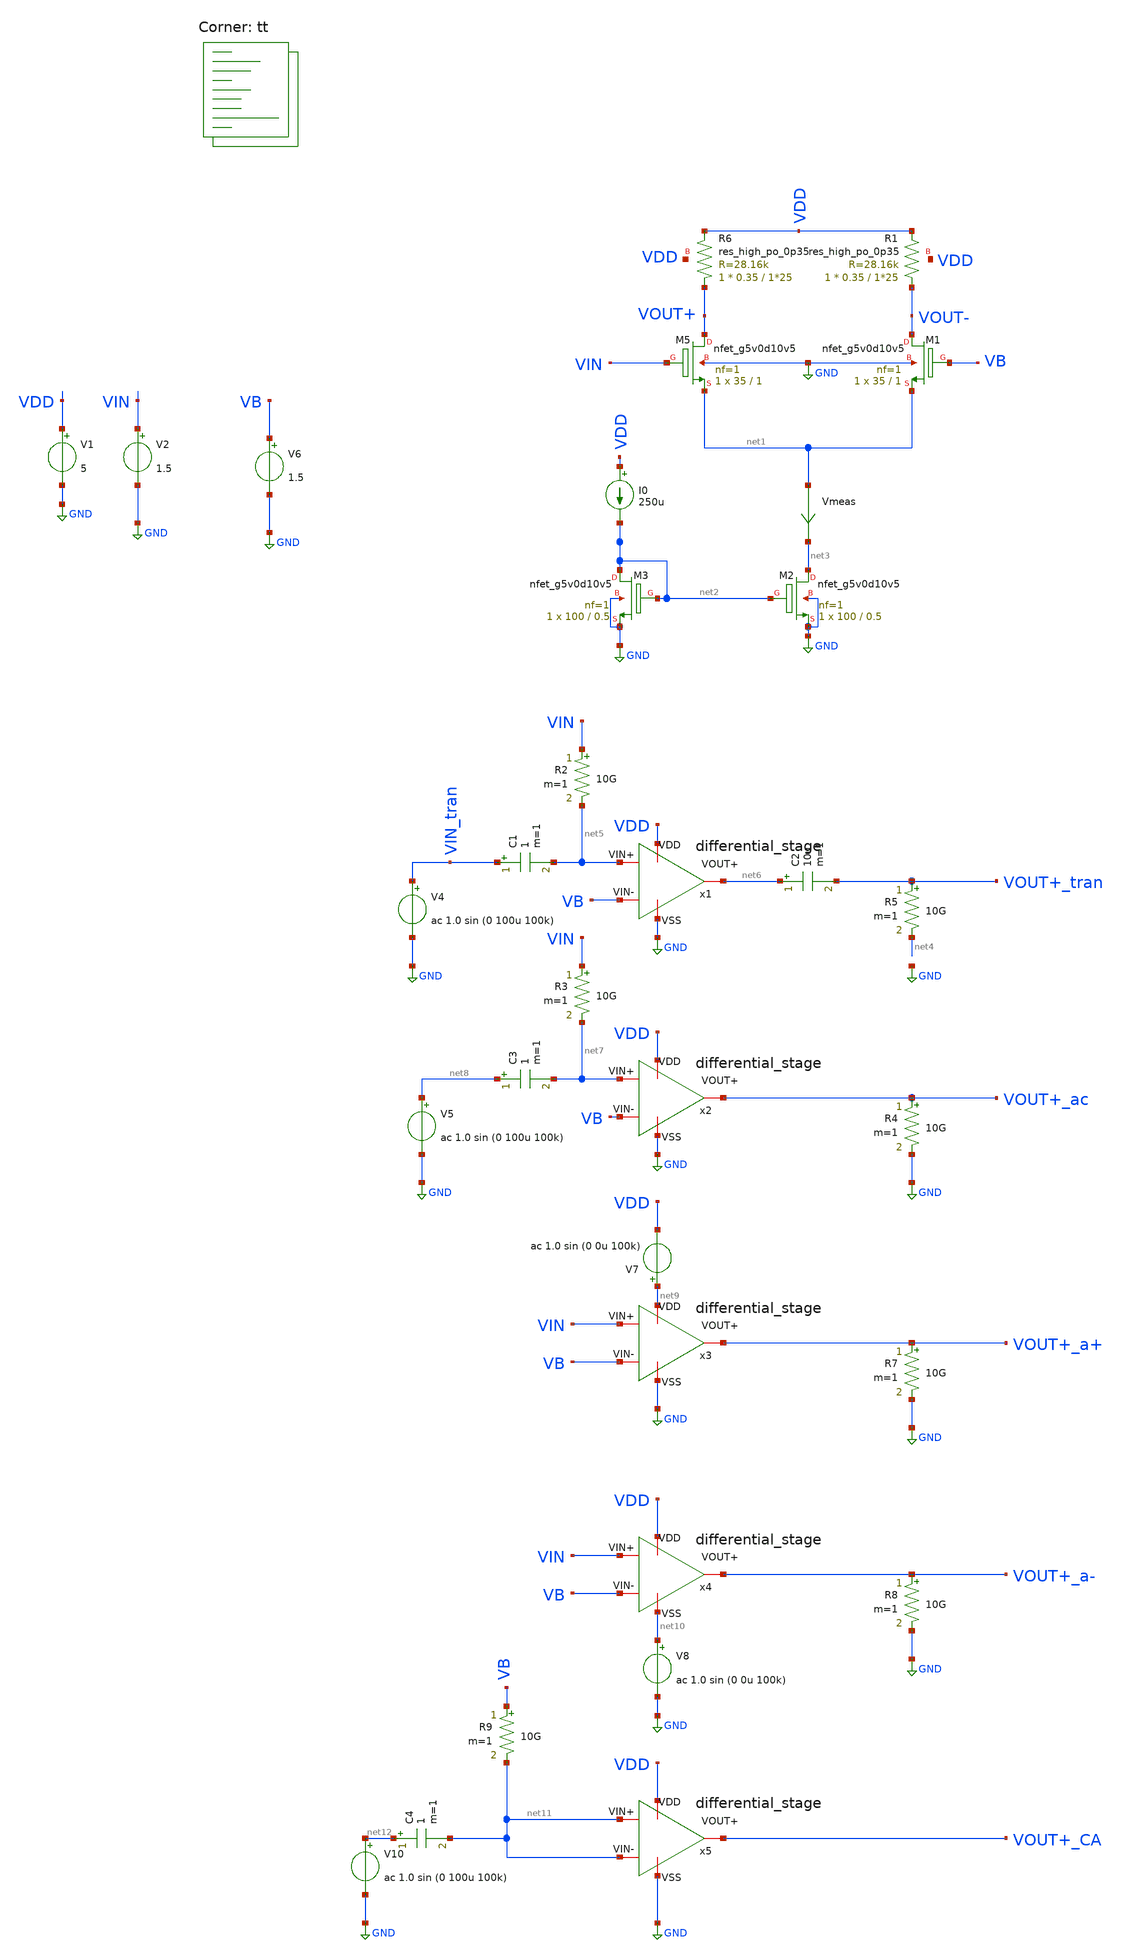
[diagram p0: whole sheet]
** sch_path: old stuff/amplifiers/differencial_stage_amps/basic_stages/basic_NMOS_resistive_stage/diferential_stage.sch
**.subckt diferential_stage
XM5 VOUT+ VIN net1 GND sky130_fd_pr__nfet_g5v0d10v5 L=1 W=35 nf=1 ad='int((1 + 1)/2) * 35 / 1 * 0.29'
+ as='int((1 + 2)/2) * 35 / 1 * 0.29' pd='2*int((1 + 1)/2) * (35 / 1 + 0.29)' ps='2*int((1 + 2)/2) * (35 / 1 + 0.29)'
+ nrd='0.29 / 35 ' nrs='0.29 / 35 ' sa=0 sb=0 sd=0 mult=1 m=1
XM1 VOUT- VB net1 GND sky130_fd_pr__nfet_g5v0d10v5 L=1 W=35 nf=1 ad='int((1 + 1)/2) * 35 / 1 * 0.29'
+ as='int((1 + 2)/2) * 35 / 1 * 0.29' pd='2*int((1 + 1)/2) * (35 / 1 + 0.29)' ps='2*int((1 + 2)/2) * (35 / 1 + 0.29)'
+ nrd='0.29 / 35 ' nrs='0.29 / 35 ' sa=0 sb=0 sd=0 mult=1 m=1
XR6 VOUT+ VDD VDD sky130_fd_pr__res_high_po_0p35 L=1*25 mult=1 m=1
XR1 VOUT- VDD VDD sky130_fd_pr__res_high_po_0p35 L=1*25 mult=1 m=1
V1 VDD GND 5
V2 VIN GND 1.5
V6 VB GND 1.5
XM2 net3 net2 GND GND sky130_fd_pr__nfet_g5v0d10v5 L=0.5 W=100 nf=1 ad='int((1 + 1)/2) * 100 / 1 * 0.29'
+ as='int((1 + 2)/2) * 100 / 1 * 0.29' pd='2*int((1 + 1)/2) * (100 / 1 + 0.29)' ps='2*int((1 + 2)/2) * (100 / 1 + 0.29)'
+ nrd='0.29 / 100 ' nrs='0.29 / 100 ' sa=0 sb=0 sd=0 mult=1 m=1
Vmeas net1 net3 0
.save i(vmeas)
R5 VOUT+_tran net4 10G m=1
R2 VIN net5 10G m=1
V4 VIN_tran GND ac 1.0 sin (0 100u 100k)
C2 net6 VOUT+_tran 10u m=1
C1 VIN_tran net5 1 m=1
R3 VIN net7 10G m=1
C3 net8 net7 1 m=1
V5 net8 GND ac 1.0 sin (0 100u 100k)
R4 VOUT+_ac GND 10G m=1
V7 net9 VDD ac 1.0 sin (0 0u 100k)
R7 VOUT+_a+ GND 10G m=1
V8 net10 GND ac 1.0 sin (0 0u 100k)
R8 VOUT+_a- GND 10G m=1
R9 VB net11 10G m=1
C4 net12 net11 1 m=1
V10 net12 GND ac 1.0 sin (0 100u 100k)
XM3 net2 net2 GND GND sky130_fd_pr__nfet_g5v0d10v5 L=0.5 W=100 nf=1 ad='int((1 + 1)/2) * 100 / 1 * 0.29'
+ as='int((1 + 2)/2) * 100 / 1 * 0.29' pd='2*int((1 + 1)/2) * (100 / 1 + 0.29)' ps='2*int((1 + 2)/2) * (100 / 1 + 0.29)'
+ nrd='0.29 / 100 ' nrs='0.29 / 100 ' sa=0 sb=0 sd=0 mult=1 m=1
I0 VDD net2 250u
x1 VDD GND net5 VB net6 differential_stage
x2 VDD GND net7 VB VOUT+_ac differential_stage
x3 net9 GND VIN VB VOUT+_a+ differential_stage
x4 VDD net10 VIN VB VOUT+_a- differential_stage
x5 VDD GND net11 net11 VOUT+_CA differential_stage
**** begin user architecture code

**************************************************************
**************************************************************
**************************************************************
**************************************************************
**************************************************************
*LIBs*********************************************************
**************************************************************
**************************************************************
**************************************************************
**************************************************************
**************************************************************
*.lib $::SKYWATER_MODELS/sky130.lib.spice tt
* chose the corners in the corner file
* tt_mm for mismatch
* ss ff sf fs standart corners
* ll hh lh hl capacitor and resistors corners
* mc for total process variation including corners
**************************************************************
**************************************************************
**************************************************************
**************************************************************
**************************************************************
*Corners/montecarlo options***********************************
**************************************************************
**************************************************************
**************************************************************
**************************************************************
**************************************************************
.TEMP 27
**************************************************************
**************************************************************
**************************************************************
**************************************************************
*SIMULATION and Plots*****************************************
**************************************************************
**************************************************************
**************************************************************
**************************************************************
.control
save all
dc V2 0 5 0.01
*dc simulation
plot v(VOUT-) v(VIN) deriv(v(VOUT-)) v(VOUT+) deriv(v(VOUT+))
*ploting VIN VOUT and the voltage gain
plot i(Vmeas)
*ploting the current for curiosity
tran 0.5ns 20u
*transient simulation
plot (v(VOUT+_tran)) v(VIN_tran)
*simple plot to exemplify the gain
fft v(VOUT+_tran) v(VIN_tran)
*fast fourier transfor
plot mag(v(VOUT+_tran)) mag(v(VIN_tran))
ac dec 20 1 1000G
*simple ac simulation
plot db(v(VOUT+_ac))
plot db(v(VOUT+_a+))
plot db(v(VOUT+_a-))
plot db(v(VOUT+_CA))
plot db((v(VOUT+_ac))/(v(VOUT+_CA)))
plot db((v(VOUT+_ac))/(v(VOUT+_a+)))
plot db((v(VOUT+_ac))/(v(VOUT+_a-)))
.endc

.lib $::SKYWATER_MODELS/sky130.lib.spice tt
**** end user architecture code
**.ends

* expanding   symbol:
*+  /home/vasco/Desktop/sky130A/amplifiers/differencial_stage_amps/basic_stages/basic_NMOS_resistive_stage/differential_stage.sym # of pins=5
** sym_path: old stuff/amplifiers/differencial_stage_amps/basic_stages/basic_NMOS_LOAD_curr_stage/differential_stage.sym
** sch_path: old stuff/amplifiers/differencial_stage_amps/basic_stages/basic_NMOS_LOAD_curr_stage/differential_stage.sch
.subckt differential_stage VDD VSS VIN+ VIN- VOUT+
*.iopin VDD
*.iopin VSS
*.iopin VIN+
*.iopin VIN-
*.iopin VOUT+
XM5 VOUT+ VIN+ net1 VSS sky130_fd_pr__nfet_g5v0d10v5 L=0.7 W=50 nf=1 ad='int((1 + 1)/2) * 50 / 1 * 0.29'
+ as='int((1 + 2)/2) * 50 / 1 * 0.29' pd='2*int((1 + 1)/2) * (50 / 1 + 0.29)' ps='2*int((1 + 2)/2) * (50 / 1 + 0.29)'
+ nrd='0.29 / 50 ' nrs='0.29 / 50 ' sa=0 sb=0 sd=0 mult=1 m=1
XM1 VOUT- VIN- net1 VSS sky130_fd_pr__nfet_g5v0d10v5 L=0.7 W=50 nf=1 ad='int((1 + 1)/2) * 50 / 1 * 0.29'
+ as='int((1 + 2)/2) * 50 / 1 * 0.29' pd='2*int((1 + 1)/2) * (50 / 1 + 0.29)' ps='2*int((1 + 2)/2) * (50 / 1 + 0.29)'
+ nrd='0.29 / 50 ' nrs='0.29 / 50 ' sa=0 sb=0 sd=0 mult=1 m=1
XM2 net1 net2 VSS VSS sky130_fd_pr__nfet_g5v0d10v5 L=0.5 W=100 nf=1 ad='int((1 + 1)/2) * 100 / 1 * 0.29'
+ as='int((1 + 2)/2) * 100 / 1 * 0.29' pd='2*int((1 + 1)/2) * (100 / 1 + 0.29)' ps='2*int((1 + 2)/2) * (100 / 1 + 0.29)'
+ nrd='0.29 / 100 ' nrs='0.29 / 100 ' sa=0 sb=0 sd=0 mult=1 m=1
XM3 net2 net2 VSS VSS sky130_fd_pr__nfet_g5v0d10v5 L=0.5 W=100 nf=1 ad='int((1 + 1)/2) * 100 / 1 * 0.29'
+ as='int((1 + 2)/2) * 100 / 1 * 0.29' pd='2*int((1 + 1)/2) * (100 / 1 + 0.29)' ps='2*int((1 + 2)/2) * (100 / 1 + 0.29)'
+ nrd='0.29 / 100 ' nrs='0.29 / 100 ' sa=0 sb=0 sd=0 mult=1 m=1
I0 VDD net2 300u
XM9 VOUT+ VB2 VDD VDD sky130_fd_pr__pfet_g5v0d10v5 L=1 W=15 nf=1 ad='int((1 + 1)/2) * 15 / 1 * 0.29'
+ as='int((1 + 2)/2) * 15 / 1 * 0.29' pd='2*int((1 + 1)/2) * (15 / 1 + 0.29)' ps='2*int((1 + 2)/2) * (15 / 1 + 0.29)'
+ nrd='0.29 / 15 ' nrs='0.29 / 15 ' sa=0 sb=0 sd=0 mult=1 m=1
XM4 VOUT- VB2 VDD VDD sky130_fd_pr__pfet_g5v0d10v5 L=1 W=15 nf=1 ad='int((1 + 1)/2) * 15 / 1 * 0.29'
+ as='int((1 + 2)/2) * 15 / 1 * 0.29' pd='2*int((1 + 1)/2) * (15 / 1 + 0.29)' ps='2*int((1 + 2)/2) * (15 / 1 + 0.29)'
+ nrd='0.29 / 15 ' nrs='0.29 / 15 ' sa=0 sb=0 sd=0 mult=1 m=1
V3 VB2 GND 3.8
.ends

.GLOBAL GND
.end
